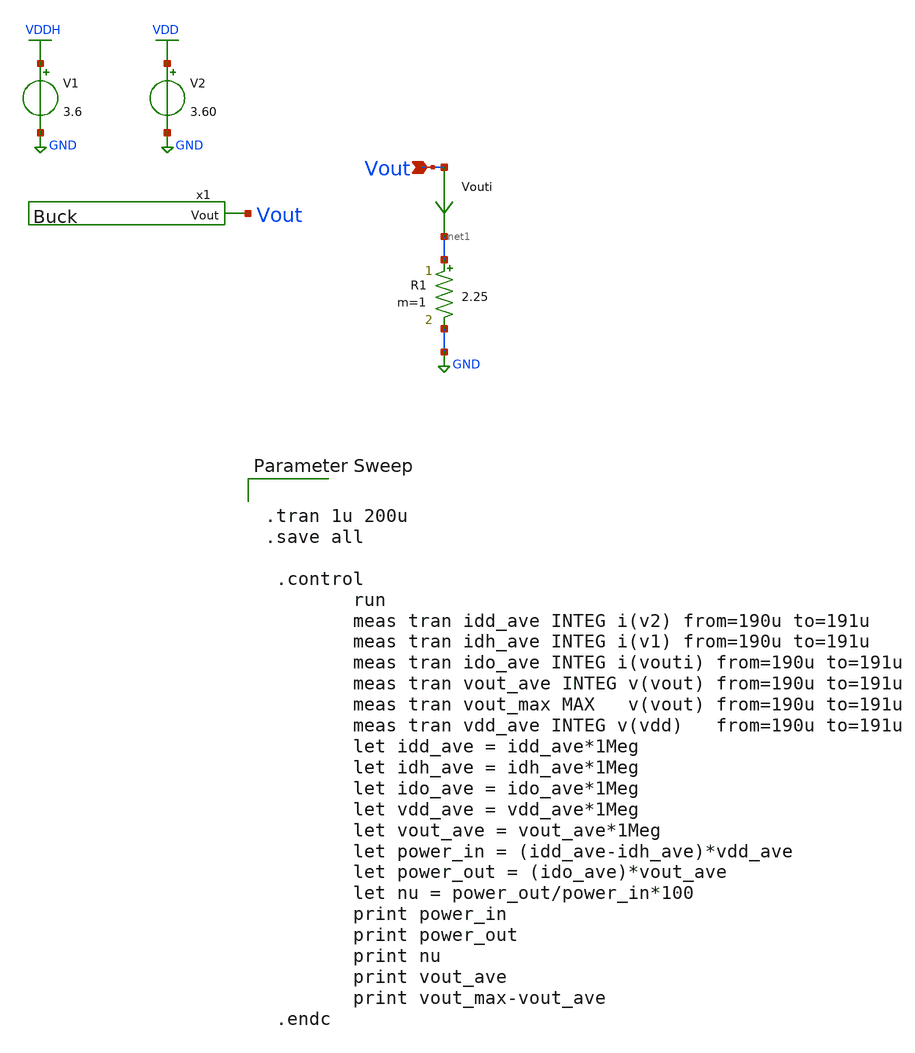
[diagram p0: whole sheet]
** sch_path: Ene_Thompson/test_Buck.sch
**.subckt test_Buck Vout
*.ipin Vout
x1 Vout Buck
V1 VDDH GND 3.6
R1 net1 GND 2.25 m=1
V2 VDD GND 3.60
Vouti Vout net1 0
.save i(vouti)
**** begin user architecture code

.lib $::SKYWATER_MODELS/sky130.lib.spice tt


.tran 1u 200u
.save all

 .control
        run
        meas tran idd_ave INTEG i(v2) from=190u to=191u
        meas tran idh_ave INTEG i(v1) from=190u to=191u
        meas tran ido_ave INTEG i(vouti) from=190u to=191u
        meas tran vout_ave INTEG v(vout) from=190u to=191u
        meas tran vout_max MAX   v(vout) from=190u to=191u
        meas tran vdd_ave INTEG v(vdd)   from=190u to=191u
        let idd_ave = idd_ave*1Meg
        let idh_ave = idh_ave*1Meg
        let ido_ave = ido_ave*1Meg
        let vdd_ave = vdd_ave*1Meg
        let vout_ave = vout_ave*1Meg
        let power_in = (idd_ave-idh_ave)*vdd_ave
        let power_out = (ido_ave)*vout_ave
        let nu = power_out/power_in*100
        print power_in
        print power_out
        print nu
        print vout_ave
        print vout_max-vout_ave
 .endc


**** end user architecture code
**.ends

* expanding   symbol:  Buck.sym # of pins=1
** sym_path: Ene_Thompson/Buck.sym
** sch_path: Ene_Thompson/Buck.sch
.subckt Buck Vout
*.opin Vout
XM1 vl psw_driven net1 VDD sky130_fd_pr__pfet_g5v0d10v5 L=0.5 W=20 nf=1 ad='int((nf+1)/2) * W/nf * 0.29'
+ as='int((nf+2)/2) * W/nf * 0.29' pd='2*int((nf+1)/2) * (W/nf + 0.29)' ps='2*int((nf+2)/2) * (W/nf + 0.29)'
+ nrd='0.29 / W' nrs='0.29 / W' sa=0 sb=0 sd=0 mult=1581 m=1581
Xx3 vl nsw_driven net4 GND sky130_fd_pr__nfet_g5v0d10v5 L=0.5 W=20 nf=1 ad='int((nf+1)/2) * W/nf * 0.29'
+ as='int((nf+2)/2) * W/nf * 0.29' pd='2*int((nf+1)/2) * (W/nf + 0.29)' ps='2*int((nf+2)/2) * (W/nf + 0.29)'
+ nrd='0.29 / W' nrs='0.29 / W' sa=0 sb=0 sd=0 mult=419 m=419
L1 net3 Vout 4.7u m=1
C1 Vout net2 1u m=1
R1 vl net3 1.5m m=1
R2 GND net2 10m m=1
Vm1 VDD net1 0
.save i(vm1)
Vm2 net4 GND 0
.save i(vm2)
x1 pswitch psw_driven drive_train
x2 nswitch nsw_driven drive_train
V2 pwm GND PULSE(0 3.6 0 0.01u 0.01u 0.422u 1u)
x4 pswitch pwm nswitch deadtime
.ends


* expanding   symbol:  drive_train.sym # of pins=2
** sym_path: Ene_Thompson/drive_train.sym
** sch_path: Ene_Thompson/drive_train.sch
.subckt drive_train A Y
*.opin Y
*.ipin A
XM1 net1 A GND GND sky130_fd_pr__nfet_g5v0d10v5 L=0.5 W=1 nf=1 ad='int((nf+1)/2) * W/nf * 0.29' as='int((nf+2)/2) * W/nf * 0.29'
+ pd='2*int((nf+1)/2) * (W/nf + 0.29)' ps='2*int((nf+2)/2) * (W/nf + 0.29)' nrd='0.29 / W' nrs='0.29 / W'
+ sa=0 sb=0 sd=0 mult=7 m=7
XM2 net1 A VDD VDD sky130_fd_pr__pfet_g5v0d10v5 L=0.5 W=1 nf=1 ad='int((nf+1)/2) * W/nf * 0.29' as='int((nf+2)/2) * W/nf * 0.29'
+ pd='2*int((nf+1)/2) * (W/nf + 0.29)' ps='2*int((nf+2)/2) * (W/nf + 0.29)' nrd='0.29 / W' nrs='0.29 / W'
+ sa=0 sb=0 sd=0 mult=7 m=7
XM3 net2 net1 GND GND sky130_fd_pr__nfet_g5v0d10v5 L=0.5 W=1 nf=1 ad='int((nf+1)/2) * W/nf * 0.29' as='int((nf+2)/2) * W/nf * 0.29'
+ pd='2*int((nf+1)/2) * (W/nf + 0.29)' ps='2*int((nf+2)/2) * (W/nf + 0.29)' nrd='0.29 / W' nrs='0.29 / W'
+ sa=0 sb=0 sd=0 mult=50 m=50
XM4 net2 net1 VDD VDD sky130_fd_pr__pfet_g5v0d10v5 L=0.5 W=1 nf=1 ad='int((nf+1)/2) * W/nf * 0.29' as='int((nf+2)/2) * W/nf * 0.29'
+ pd='2*int((nf+1)/2) * (W/nf + 0.29)' ps='2*int((nf+2)/2) * (W/nf + 0.29)' nrd='0.29 / W' nrs='0.29 / W'
+ sa=0 sb=0 sd=0 mult=50 m=50
XM5 net3 net2 GND GND sky130_fd_pr__nfet_g5v0d10v5 L=0.5 W=10 nf=1 ad='int((nf+1)/2) * W/nf * 0.29' as='int((nf+2)/2) * W/nf * 0.29'
+ pd='2*int((nf+1)/2) * (W/nf + 0.29)' ps='2*int((nf+2)/2) * (W/nf + 0.29)' nrd='0.29 / W' nrs='0.29 / W'
+ sa=0 sb=0 sd=0 mult=35 m=35
XM6 net3 net2 VDD VDD sky130_fd_pr__pfet_g5v0d10v5 L=0.5 W=10 nf=1 ad='int((nf+1)/2) * W/nf * 0.29' as='int((nf+2)/2) * W/nf * 0.29'
+ pd='2*int((nf+1)/2) * (W/nf + 0.29)' ps='2*int((nf+2)/2) * (W/nf + 0.29)' nrd='0.29 / W' nrs='0.29 / W'
+ sa=0 sb=0 sd=0 mult=35 m=35
XM7 Y net3 GND GND sky130_fd_pr__nfet_g5v0d10v5 L=0.5 W=20 nf=1 ad='int((nf+1)/2) * W/nf * 0.29' as='int((nf+2)/2) * W/nf * 0.29'
+ pd='2*int((nf+1)/2) * (W/nf + 0.29)' ps='2*int((nf+2)/2) * (W/nf + 0.29)' nrd='0.29 / W' nrs='0.29 / W'
+ sa=0 sb=0 sd=0 mult=125 m=125
XM8 Y net3 VDD VDD sky130_fd_pr__pfet_g5v0d10v5 L=0.5 W=20 nf=1 ad='int((nf+1)/2) * W/nf * 0.29' as='int((nf+2)/2) * W/nf * 0.29'
+ pd='2*int((nf+1)/2) * (W/nf + 0.29)' ps='2*int((nf+2)/2) * (W/nf + 0.29)' nrd='0.29 / W' nrs='0.29 / W'
+ sa=0 sb=0 sd=0 mult=125 m=125
.ends


* expanding   symbol:  deadtime.sym # of pins=3
** sym_path: Ene_Thompson/deadtime.sym
** sch_path: Ene_Thompson/deadtime.sch
.subckt deadtime highside pwm lowside
*.ipin pwm
*.opin highside
*.opin lowside
x1 pwm low_fb VGND VNB VPB VPWR high1 sky130_fd_sc_hd__nand2_1
x2 high_fb pwm_n VGND VNB VPB VPWR low1 sky130_fd_sc_hd__nand2_1
x3 high1 VGND VNB VPB VPWR high2 sky130_fd_sc_hd__inv_1
x4 high2 VGND VNB VPB VPWR high3 sky130_fd_sc_hd__inv_1
x5 high3 VGND VNB VPB VPWR highside sky130_fd_sc_hd__inv_1
x6 highside VGND VNB VPB VPWR high_fb sky130_fd_sc_hd__inv_1
x7 low1 VGND VNB VPB VPWR low2 sky130_fd_sc_hd__inv_1
x8 low2 VGND VNB VPB VPWR lowside sky130_fd_sc_hd__inv_1
x9 lowside VGND VNB VPB VPWR low4 sky130_fd_sc_hd__inv_1
x10 low4 VGND VNB VPB VPWR low_fb sky130_fd_sc_hd__inv_1
x11 pwm VGND VNB VPB VPWR pwm_n sky130_fd_sc_hd__inv_1
.ends

.GLOBAL VDDH
.GLOBAL GND
.GLOBAL VDD
.end
